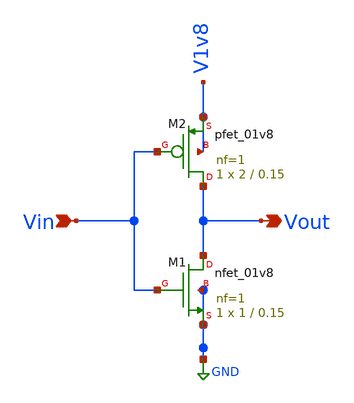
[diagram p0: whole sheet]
** sch_path: xschem/StandardCells/Inverter1v8.sch
**.subckt Inverter1v8 Vout Vin
*.opin Vout
*.ipin Vin
XM1 Vout Vin GND GND sky130_fd_pr__nfet_01v8 L=0.15 W=1 nf=1 ad='int((nf+1)/2) * W/nf * 0.29' as='int((nf+2)/2) * W/nf * 0.29'
+ pd='2*int((nf+1)/2) * (W/nf + 0.29)' ps='2*int((nf+2)/2) * (W/nf + 0.29)' nrd='0.29 / W' nrs='0.29 / W'
+ sa=0 sb=0 sd=0 mult=1 m=1
XM2 Vout Vin V1v8 V1v8 sky130_fd_pr__pfet_01v8 L=0.15 W=2 nf=1 ad='int((nf+1)/2) * W/nf * 0.29' as='int((nf+2)/2) * W/nf * 0.29'
+ pd='2*int((nf+1)/2) * (W/nf + 0.29)' ps='2*int((nf+2)/2) * (W/nf + 0.29)' nrd='0.29 / W' nrs='0.29 / W'
+ sa=0 sb=0 sd=0 mult=1 m=1
**.ends
.GLOBAL GND
.end
